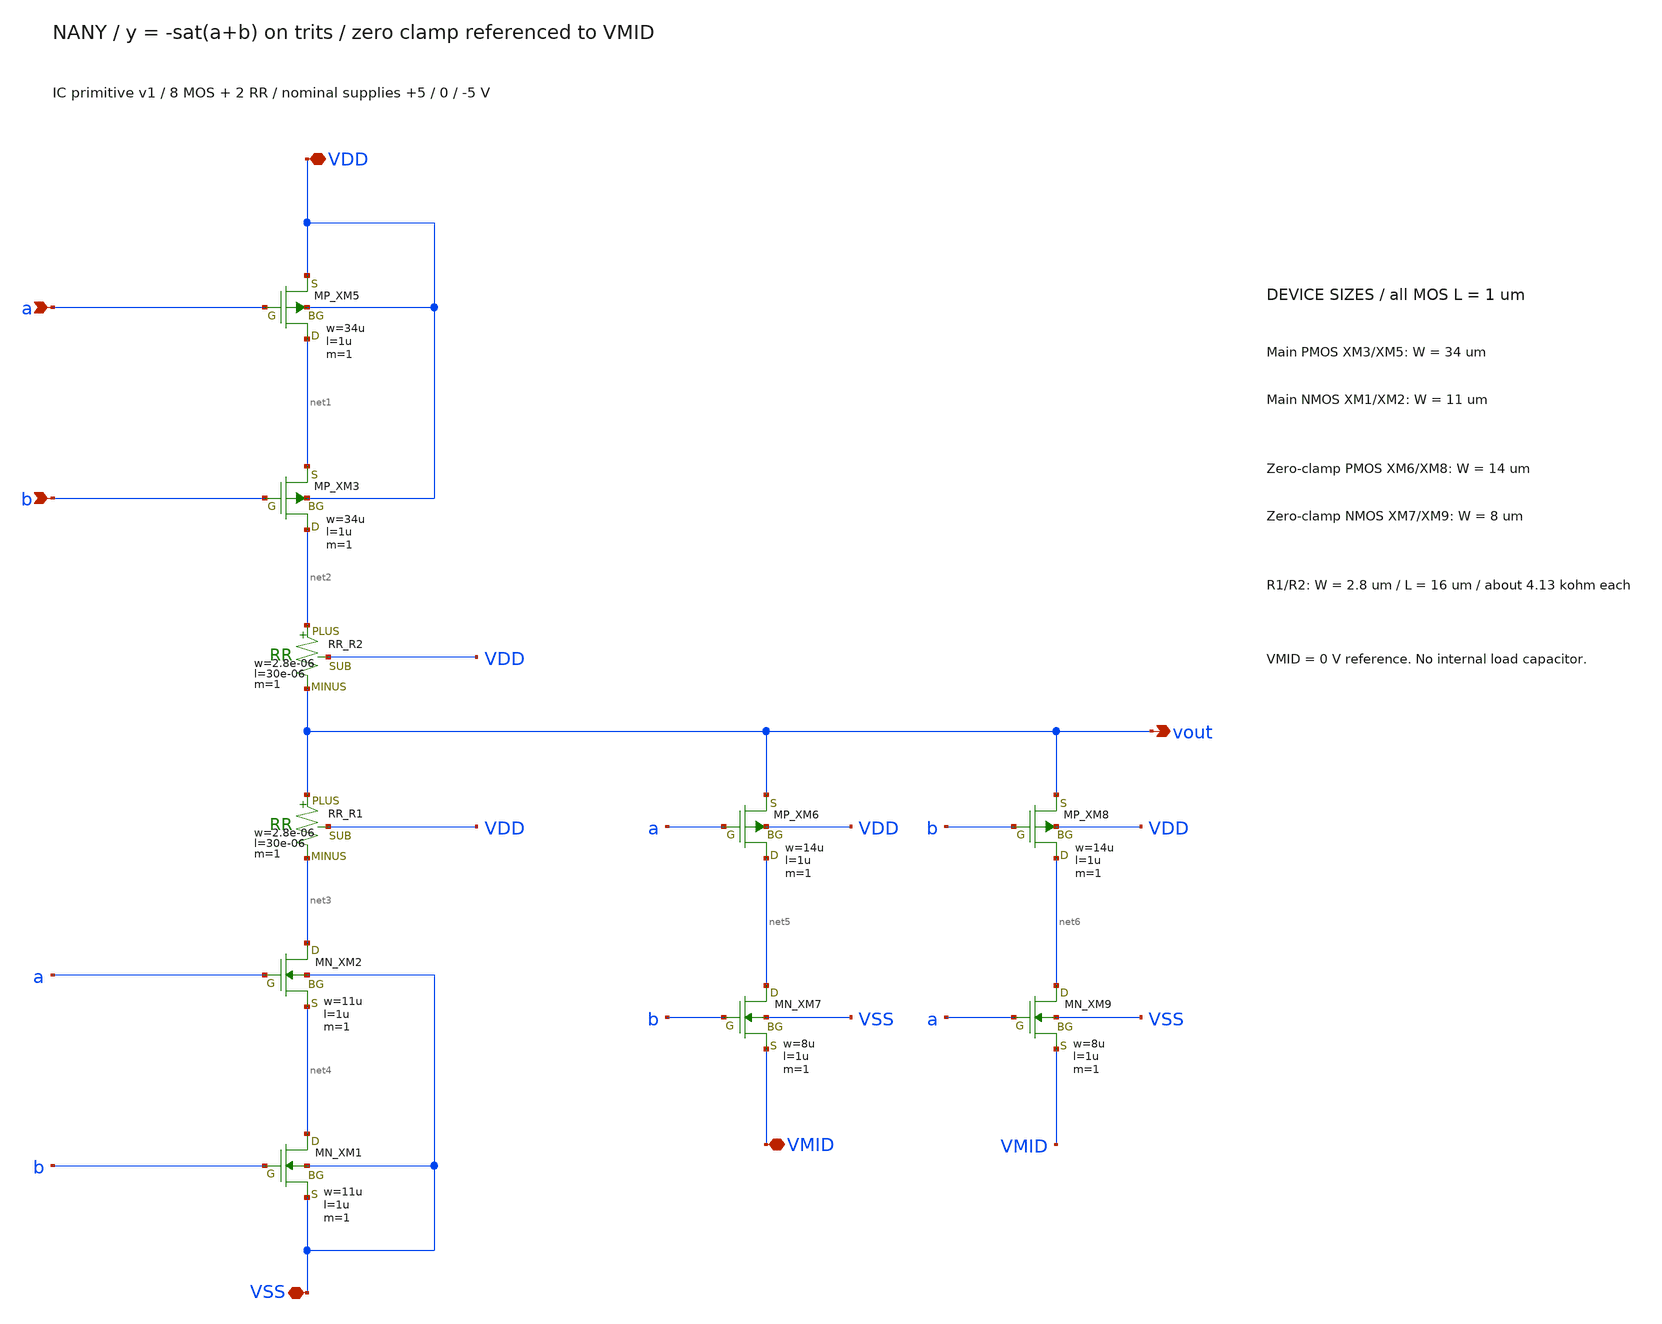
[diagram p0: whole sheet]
** sch_path: member_project/balanced-ternary-logic/PenguinEino/submission/nany.sch
**.subckt nany VDD a b vout VSS VMID
*.iopin VDD
*.ipin a
*.ipin b
*.opin vout
*.iopin VSS
*.iopin VMID
XXM3 net2 b net1 VDD PMOS w=34u l=1u nrd=0 nrs=0 m=1
XR2 net2 vout VDD F_RR w=2.8e-06 l=30e-06 R=1 tc1=0 tc2=0 m=1
XR1 vout net3 VDD F_RR w=2.8e-06 l=30e-06 R=1 tc1=0 tc2=0 m=1
XXM2 net3 a net4 VSS NMOS w=11u l=1u nrd=0 nrs=0 m=1
XXM1 net4 b VSS VSS NMOS w=11u l=1u nrd=0 nrs=0 m=1
XXM5 net1 a VDD VDD PMOS w=34u l=1u nrd=0 nrs=0 m=1
XXM6 net5 a vout VDD PMOS w=14u l=1u nrd=0 nrs=0 m=1
XXM7 net5 b VMID VSS NMOS w=8u l=1u nrd=0 nrs=0 m=1
XXM8 net6 b vout VDD PMOS w=14u l=1u nrd=0 nrs=0 m=1
XXM9 net6 a VMID VSS NMOS w=8u l=1u nrd=0 nrs=0 m=1
**.ends
.end
